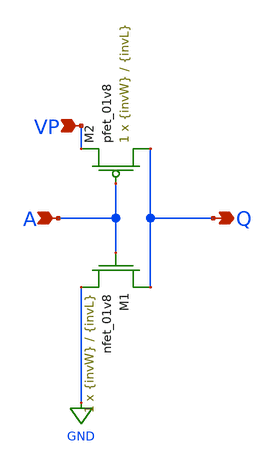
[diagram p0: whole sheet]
** sch_path: schemas/n_inv.sch
**.subckt n_inv A VP Q
*.ipin A
*.ipin VP
*.opin Q
XM1 Q A GND GND sky130_fd_pr__nfet_01v8 L={invL} W={invW} nf=1 ad='int((nf+1)/2) * W/nf * 0.29' as='int((nf+2)/2) * W/nf * 0.29'
+ pd='2*int((nf+1)/2) * (W/nf + 0.29)' ps='2*int((nf+2)/2) * (W/nf + 0.29)' nrd='0.29 / W' nrs='0.29 / W'
+ sa=0 sb=0 sd=0 mult=1 m=1
XM2 Q A VP VDD sky130_fd_pr__pfet_01v8 L={invL} W={invW} nf=1 ad='int((nf+1)/2) * W/nf * 0.29' as='int((nf+2)/2) * W/nf * 0.29'
+ pd='2*int((nf+1)/2) * (W/nf + 0.29)' ps='2*int((nf+2)/2) * (W/nf + 0.29)' nrd='0.29 / W' nrs='0.29 / W'
+ sa=0 sb=0 sd=0 mult=1 m=1
**.ends
.GLOBAL GND
.end
